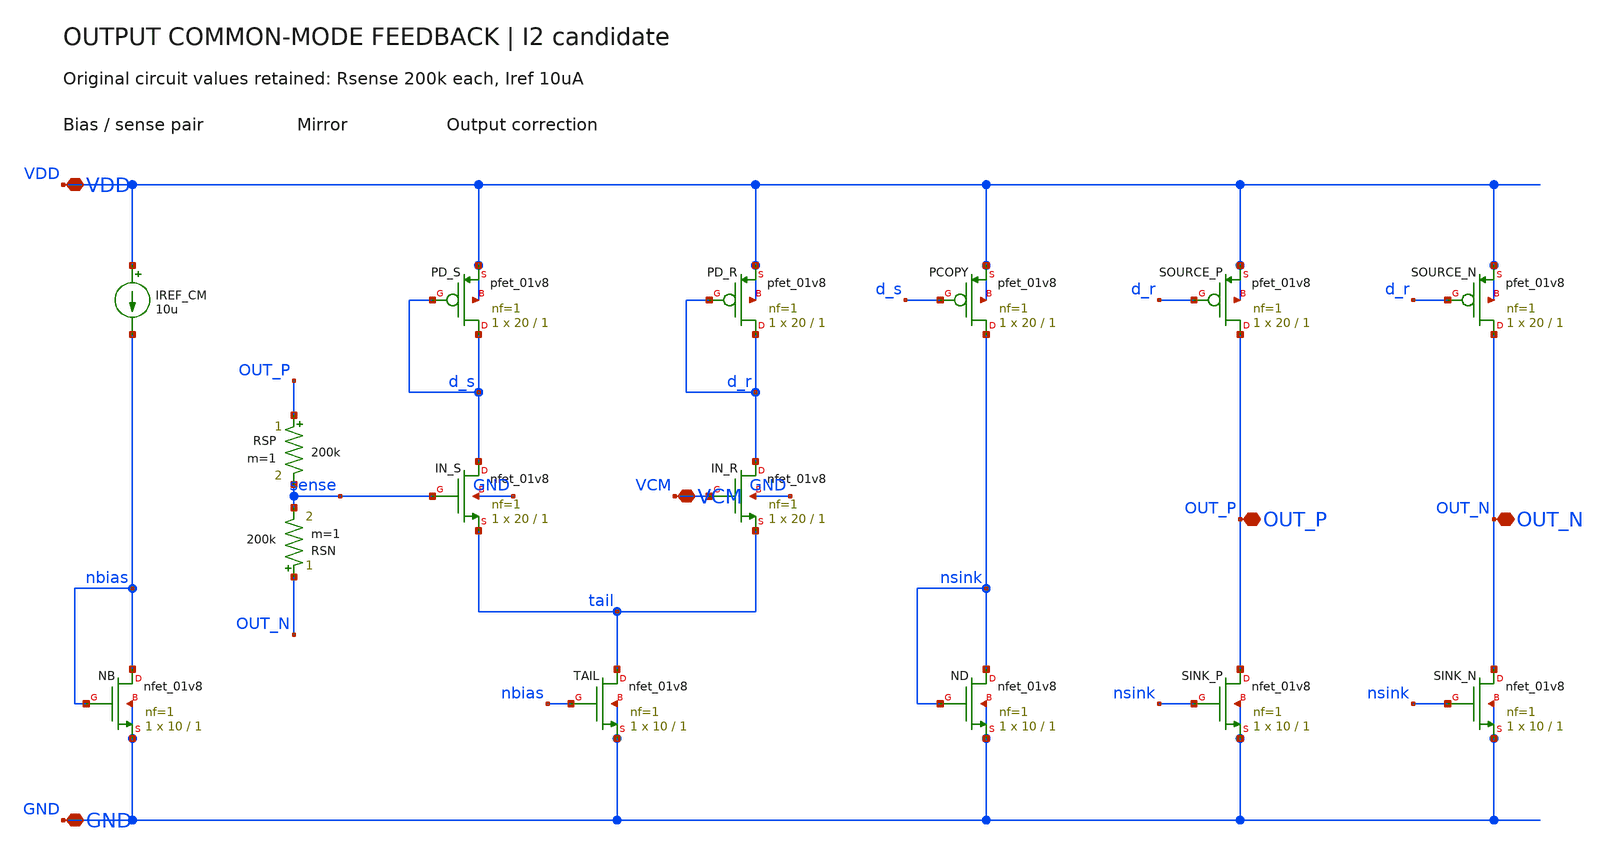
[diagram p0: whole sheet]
** sch_path: blocks/02_CMFB/xschem/CMFB_OUT_I2_Wired.sch
**.subckt CMFB_OUT_I2_Wired VDD GND OUT_P OUT_N VCM
*.iopin VDD
*.iopin GND
*.iopin OUT_P
*.iopin OUT_N
*.iopin VCM
XNB nbias nbias GND GND sky130_fd_pr__nfet_01v8 L=1 W=10 nf=1 mult=1 ad=2.9 as=2.9 pd=20.58 ps=20.58
+ nrd=0.029 nrs=0.029 sa=0 sb=0 sd=0
XTAIL tail nbias GND GND sky130_fd_pr__nfet_01v8 L=1 W=10 nf=1 mult=1 ad=2.9 as=2.9 pd=20.58
+ ps=20.58 nrd=0.029 nrs=0.029 sa=0 sb=0 sd=0
XIN_S d_s sense tail GND sky130_fd_pr__nfet_01v8 L=1 W=20 nf=1 mult=1 ad=5.8 as=5.8 pd=40.58
+ ps=40.58 nrd=0.0145 nrs=0.0145 sa=0 sb=0 sd=0
XIN_R d_r VCM tail GND sky130_fd_pr__nfet_01v8 L=1 W=20 nf=1 mult=1 ad=5.8 as=5.8 pd=40.58 ps=40.58
+ nrd=0.0145 nrs=0.0145 sa=0 sb=0 sd=0
XPD_S d_s d_s VDD VDD sky130_fd_pr__pfet_01v8 L=1 W=20 nf=1 mult=1 ad=5.8 as=5.8 pd=40.58 ps=40.58
+ nrd=0.0145 nrs=0.0145 sa=0 sb=0 sd=0
XPD_R d_r d_r VDD VDD sky130_fd_pr__pfet_01v8 L=1 W=20 nf=1 mult=1 ad=5.8 as=5.8 pd=40.58 ps=40.58
+ nrd=0.0145 nrs=0.0145 sa=0 sb=0 sd=0
XPCOPY nsink d_s VDD VDD sky130_fd_pr__pfet_01v8 L=1 W=20 nf=1 mult=1 ad=5.8 as=5.8 pd=40.58
+ ps=40.58 nrd=0.0145 nrs=0.0145 sa=0 sb=0 sd=0
XND nsink nsink GND GND sky130_fd_pr__nfet_01v8 L=1 W=10 nf=1 mult=1 ad=2.9 as=2.9 pd=20.58 ps=20.58
+ nrd=0.029 nrs=0.029 sa=0 sb=0 sd=0
XSOURCE_P OUT_P d_r VDD VDD sky130_fd_pr__pfet_01v8 L=1 W=20 nf=1 mult=1 ad=5.8 as=5.8 pd=40.58
+ ps=40.58 nrd=0.0145 nrs=0.0145 sa=0 sb=0 sd=0
XSOURCE_N OUT_N d_r VDD VDD sky130_fd_pr__pfet_01v8 L=1 W=20 nf=1 mult=1 ad=5.8 as=5.8 pd=40.58
+ ps=40.58 nrd=0.0145 nrs=0.0145 sa=0 sb=0 sd=0
XSINK_P OUT_P nsink GND GND sky130_fd_pr__nfet_01v8 L=1 W=10 nf=1 mult=1 ad=2.9 as=2.9 pd=20.58
+ ps=20.58 nrd=0.029 nrs=0.029 sa=0 sb=0 sd=0
XSINK_N OUT_N nsink GND GND sky130_fd_pr__nfet_01v8 L=1 W=10 nf=1 mult=1 ad=2.9 as=2.9 pd=20.58
+ ps=20.58 nrd=0.029 nrs=0.029 sa=0 sb=0 sd=0
IREF_CM VDD nbias 10u
RSP OUT_P sense 200k m=1
RSN OUT_N sense 200k m=1
**.ends
.end
